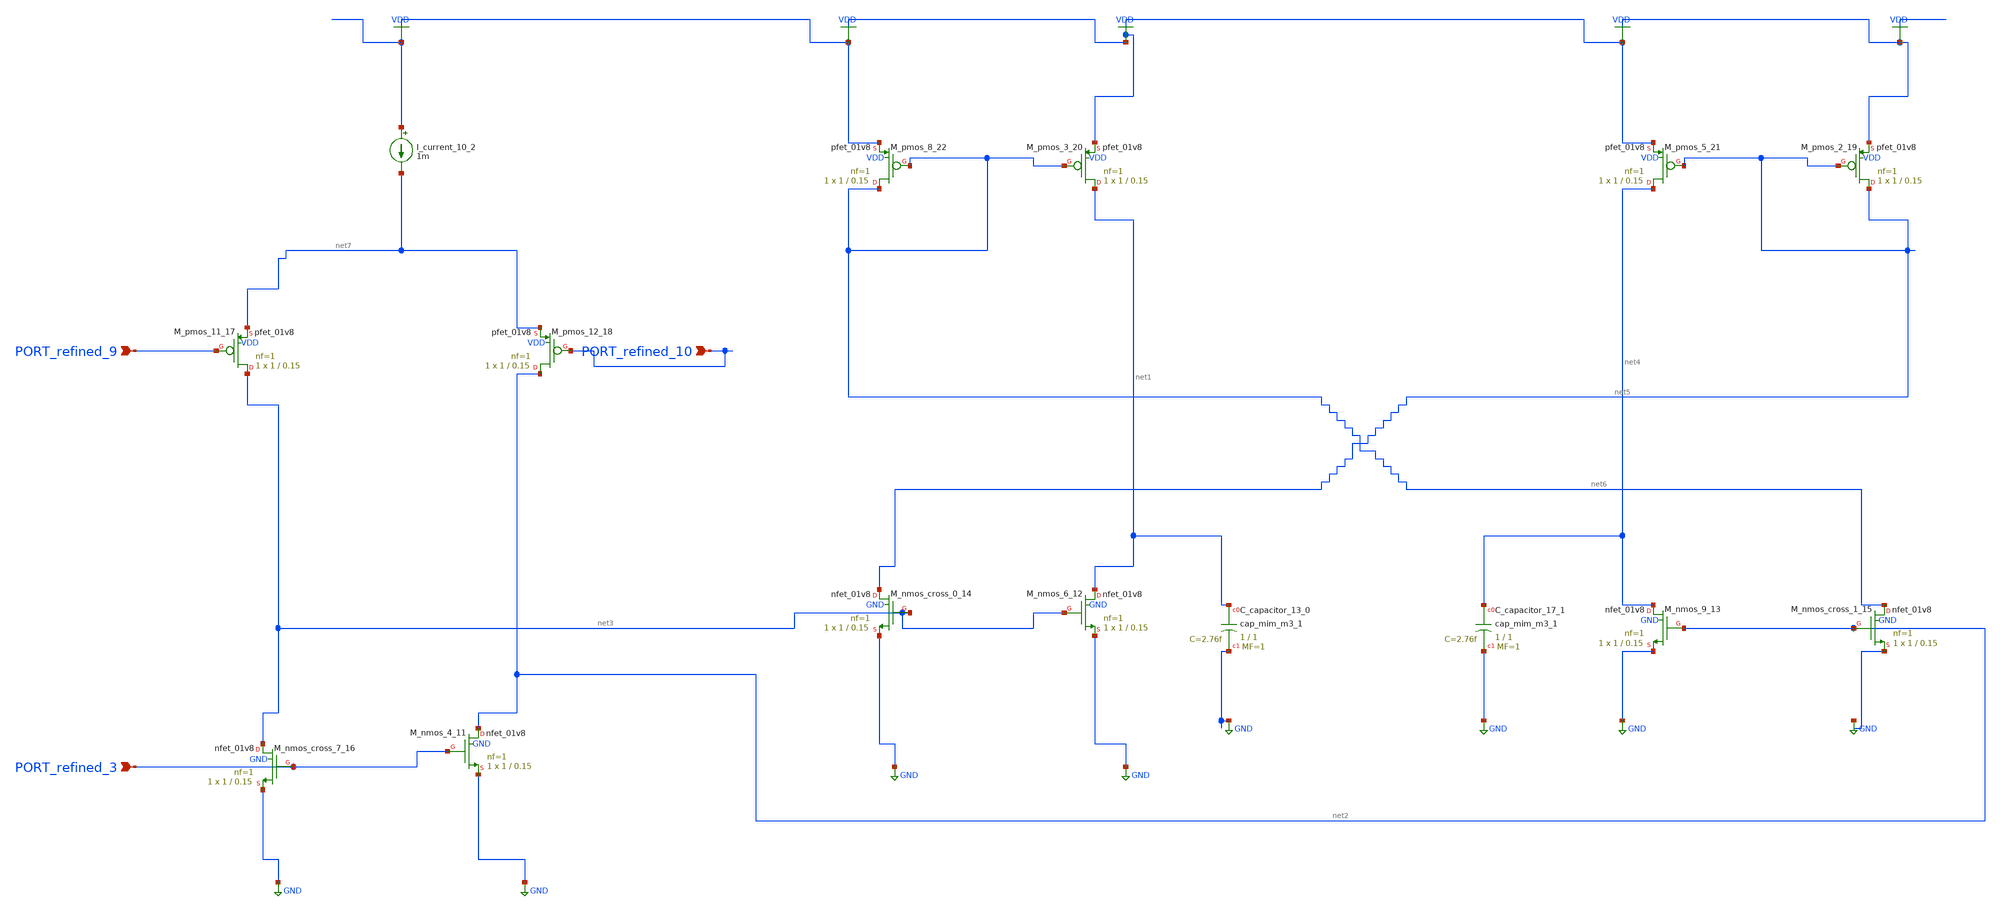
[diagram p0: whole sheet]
** sch_path: schematics/AMSNet/705.sch
**.subckt 705 PORT_refined_9 PORT_refined_3 PORT_refined_10
*.ipin PORT_refined_9
*.ipin PORT_refined_3
*.ipin PORT_refined_10
XC_capacitor_13_0 net1 GND sky130_fd_pr__cap_mim_m3_1 W=1 L=1 MF=1 m=1
XC_capacitor_17_1 net4 GND sky130_fd_pr__cap_mim_m3_1 W=1 L=1 MF=1 m=1
I_current_10_2 VDD net7 1m
XM_nmos_4_11 net2 PORT_refined_3 GND GND sky130_fd_pr__nfet_01v8 L=0.15 W=1 nf=1 ad='int((1 + 1)/2) * 1 / 1 * 0.29'
+ as='int((1 + 2)/2) * 1 / 1 * 0.29' pd='2*int((1 + 1)/2) * (1 / 1 + 0.29)' ps='2*int((1 + 2)/2) * (1 / 1 + 0.29)'
+ nrd='0.29 / 1 ' nrs='0.29 / 1 ' sa=0 sb=0 sd=0 mult=1 m=1
XM_nmos_6_12 net1 net3 GND GND sky130_fd_pr__nfet_01v8 L=0.15 W=1 nf=1 ad='int((1 + 1)/2) * 1 / 1 * 0.29'
+ as='int((1 + 2)/2) * 1 / 1 * 0.29' pd='2*int((1 + 1)/2) * (1 / 1 + 0.29)' ps='2*int((1 + 2)/2) * (1 / 1 + 0.29)'
+ nrd='0.29 / 1 ' nrs='0.29 / 1 ' sa=0 sb=0 sd=0 mult=1 m=1
XM_nmos_9_13 net4 net2 GND GND sky130_fd_pr__nfet_01v8 L=0.15 W=1 nf=1 ad='int((1 + 1)/2) * 1 / 1 * 0.29'
+ as='int((1 + 2)/2) * 1 / 1 * 0.29' pd='2*int((1 + 1)/2) * (1 / 1 + 0.29)' ps='2*int((1 + 2)/2) * (1 / 1 + 0.29)'
+ nrd='0.29 / 1 ' nrs='0.29 / 1 ' sa=0 sb=0 sd=0 mult=1 m=1
XM_nmos_cross_0_14 net5 net3 GND GND sky130_fd_pr__nfet_01v8 L=0.15 W=1 nf=1 ad='int((1 + 1)/2) * 1 / 1 * 0.29'
+ as='int((1 + 2)/2) * 1 / 1 * 0.29' pd='2*int((1 + 1)/2) * (1 / 1 + 0.29)' ps='2*int((1 + 2)/2) * (1 / 1 + 0.29)'
+ nrd='0.29 / 1 ' nrs='0.29 / 1 ' sa=0 sb=0 sd=0 mult=1 m=1
XM_nmos_cross_1_15 net6 net2 GND GND sky130_fd_pr__nfet_01v8 L=0.15 W=1 nf=1 ad='int((1 + 1)/2) * 1 / 1 * 0.29'
+ as='int((1 + 2)/2) * 1 / 1 * 0.29' pd='2*int((1 + 1)/2) * (1 / 1 + 0.29)' ps='2*int((1 + 2)/2) * (1 / 1 + 0.29)'
+ nrd='0.29 / 1 ' nrs='0.29 / 1 ' sa=0 sb=0 sd=0 mult=1 m=1
XM_nmos_cross_7_16 net3 PORT_refined_3 GND GND sky130_fd_pr__nfet_01v8 L=0.15 W=1 nf=1 ad='int((1 + 1)/2) * 1 / 1 * 0.29'
+ as='int((1 + 2)/2) * 1 / 1 * 0.29' pd='2*int((1 + 1)/2) * (1 / 1 + 0.29)' ps='2*int((1 + 2)/2) * (1 / 1 + 0.29)'
+ nrd='0.29 / 1 ' nrs='0.29 / 1 ' sa=0 sb=0 sd=0 mult=1 m=1
XM_pmos_11_17 net3 PORT_refined_9 net7 VDD sky130_fd_pr__pfet_01v8 L=0.15 W=1 nf=1 ad='int((1 + 1)/2) * 1 / 1 * 0.29'
+ as='int((1 + 2)/2) * 1 / 1 * 0.29' pd='2*int((1 + 1)/2) * (1 / 1 + 0.29)' ps='2*int((1 + 2)/2) * (1 / 1 + 0.29)'
+ nrd='0.29 / 1 ' nrs='0.29 / 1 ' sa=0 sb=0 sd=0 mult=1 m=1
XM_pmos_12_18 net2 PORT_refined_10 net7 VDD sky130_fd_pr__pfet_01v8 L=0.15 W=1 nf=1 ad='int((1 + 1)/2) * 1 / 1 * 0.29'
+ as='int((1 + 2)/2) * 1 / 1 * 0.29' pd='2*int((1 + 1)/2) * (1 / 1 + 0.29)' ps='2*int((1 + 2)/2) * (1 / 1 + 0.29)'
+ nrd='0.29 / 1 ' nrs='0.29 / 1 ' sa=0 sb=0 sd=0 mult=1 m=1
XM_pmos_2_19 net5 net5 VDD VDD sky130_fd_pr__pfet_01v8 L=0.15 W=1 nf=1 ad='int((1 + 1)/2) * 1 / 1 * 0.29'
+ as='int((1 + 2)/2) * 1 / 1 * 0.29' pd='2*int((1 + 1)/2) * (1 / 1 + 0.29)' ps='2*int((1 + 2)/2) * (1 / 1 + 0.29)'
+ nrd='0.29 / 1 ' nrs='0.29 / 1 ' sa=0 sb=0 sd=0 mult=1 m=1
XM_pmos_3_20 net1 net6 VDD VDD sky130_fd_pr__pfet_01v8 L=0.15 W=1 nf=1 ad='int((1 + 1)/2) * 1 / 1 * 0.29'
+ as='int((1 + 2)/2) * 1 / 1 * 0.29' pd='2*int((1 + 1)/2) * (1 / 1 + 0.29)' ps='2*int((1 + 2)/2) * (1 / 1 + 0.29)'
+ nrd='0.29 / 1 ' nrs='0.29 / 1 ' sa=0 sb=0 sd=0 mult=1 m=1
XM_pmos_5_21 net4 net5 VDD VDD sky130_fd_pr__pfet_01v8 L=0.15 W=1 nf=1 ad='int((1 + 1)/2) * 1 / 1 * 0.29'
+ as='int((1 + 2)/2) * 1 / 1 * 0.29' pd='2*int((1 + 1)/2) * (1 / 1 + 0.29)' ps='2*int((1 + 2)/2) * (1 / 1 + 0.29)'
+ nrd='0.29 / 1 ' nrs='0.29 / 1 ' sa=0 sb=0 sd=0 mult=1 m=1
XM_pmos_8_22 net6 net6 VDD VDD sky130_fd_pr__pfet_01v8 L=0.15 W=1 nf=1 ad='int((1 + 1)/2) * 1 / 1 * 0.29'
+ as='int((1 + 2)/2) * 1 / 1 * 0.29' pd='2*int((1 + 1)/2) * (1 / 1 + 0.29)' ps='2*int((1 + 2)/2) * (1 / 1 + 0.29)'
+ nrd='0.29 / 1 ' nrs='0.29 / 1 ' sa=0 sb=0 sd=0 mult=1 m=1
**.ends
.GLOBAL GND
.GLOBAL VDD
.end
